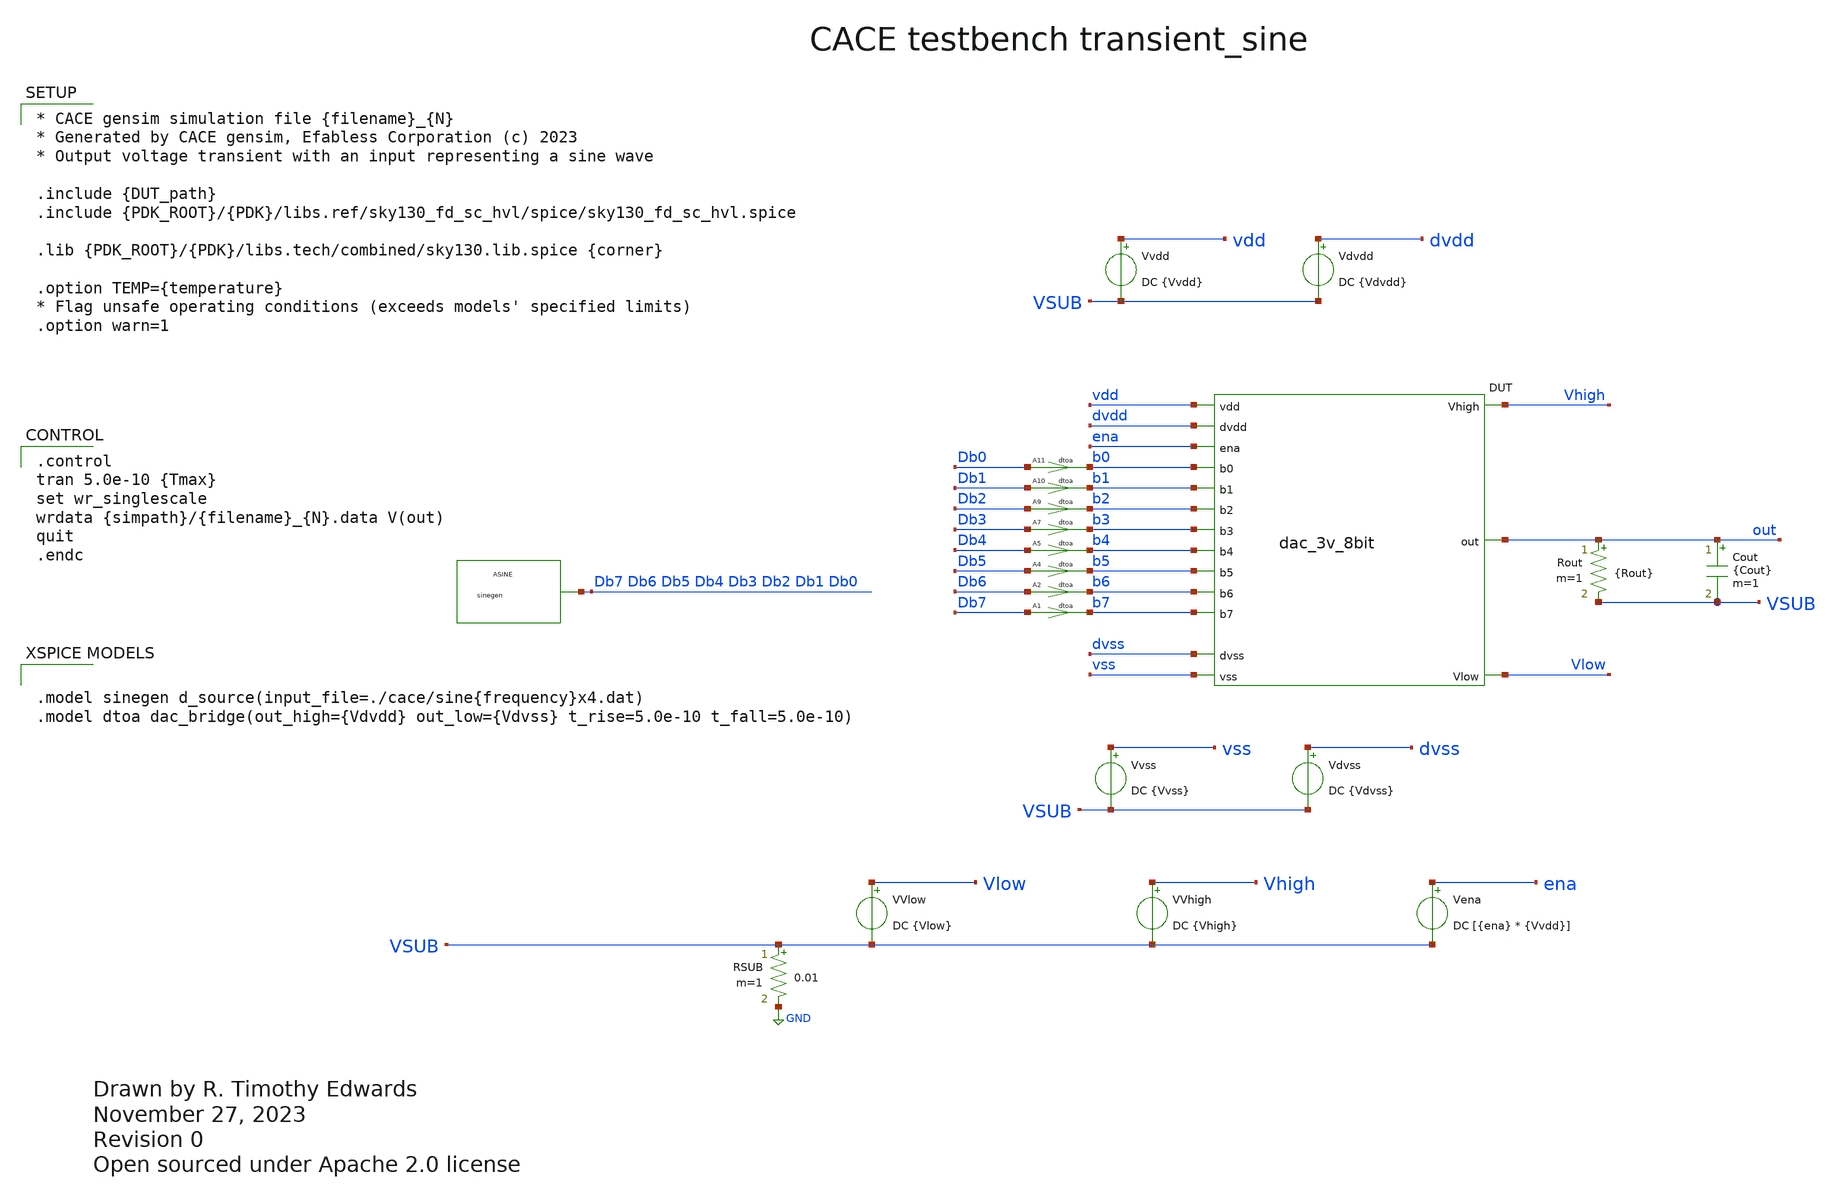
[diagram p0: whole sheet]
** sch_path: cace/transient_sine.sch
* Open sourced under Apache 2.0 license
**.subckt transient_sine
VVlow Vlow VSUB DC {Vlow}
VVhigh Vhigh VSUB DC {Vhigh}
Vena ena VSUB DC [{ena} * {Vvdd}]
Vvss vss VSUB DC {Vvss}
Rout out VSUB {Rout} m=1
Cout out VSUB {Cout} m=1
Vdvss dvss VSUB DC {Vdvss}
Vvdd vdd VSUB DC {Vvdd}
Vdvdd dvdd VSUB DC {Vdvdd}
RSUB VSUB GND 0.01 m=1
XDUT {PIN|dvdd|dvdd} {PIN|vdd|vdd} {PIN|dvss|dvss} {PIN|vss|vss} {PIN|Vhigh|Vhigh} {PIN|Vlow|Vlow} {PIN|out|out}
+ {PIN|ena|ena} {PIN|b0|b0} {PIN|b1|b1} {PIN|b2|b2} {PIN|b3|b3} {PIN|b4|b4} {PIN|b5|b5} {PIN|b6|b6} {PIN|b7|b7}
+ {DUT_name}
A1 [ Db7 ] [ b7 ] dtoa
A2 [ Db6 ] [ b6 ] dtoa
A4 [ Db5 ] [ b5 ] dtoa
A5 [ Db4 ] [ b4 ] dtoa
A7 [ Db3 ] [ b3 ] dtoa
A9 [ Db2 ] [ b2 ] dtoa
A10 [ Db1 ] [ b1 ] dtoa
A11 [ Db0 ] [ b0 ] dtoa
ASINE [ Db7 Db7 Db7 Db7 Db7 Db7 Db7 Db7 Db6 Db5 Db4 Db3 Db2 Db1 Db0 ] sinegen
**** begin user architecture code

.control
tran 5.0e-10 {Tmax}
set wr_singlescale
wrdata {simpath}/{filename}_{N}.data V(out)
quit
.endc



* CACE gensim simulation file {filename}_{N}
* Generated by CACE gensim, Efabless Corporation (c) 2023
* Output voltage transient with an input representing a sine wave

.include {DUT_path}
.include {PDK_ROOT}/{PDK}/libs.ref/sky130_fd_sc_hvl/spice/sky130_fd_sc_hvl.spice

.lib {PDK_ROOT}/{PDK}/libs.tech/combined/sky130.lib.spice {corner}

.option TEMP={temperature}
* Flag unsafe operating conditions (exceeds models' specified limits)
.option warn=1




.model sinegen d_source(input_file=./cace/sine{frequency}x4.dat)
.model dtoa dac_bridge(out_high={Vdvdd} out_low={Vdvss} t_rise=5.0e-10 t_fall=5.0e-10)


**** end user architecture code
**.ends
.GLOBAL GND
.end
